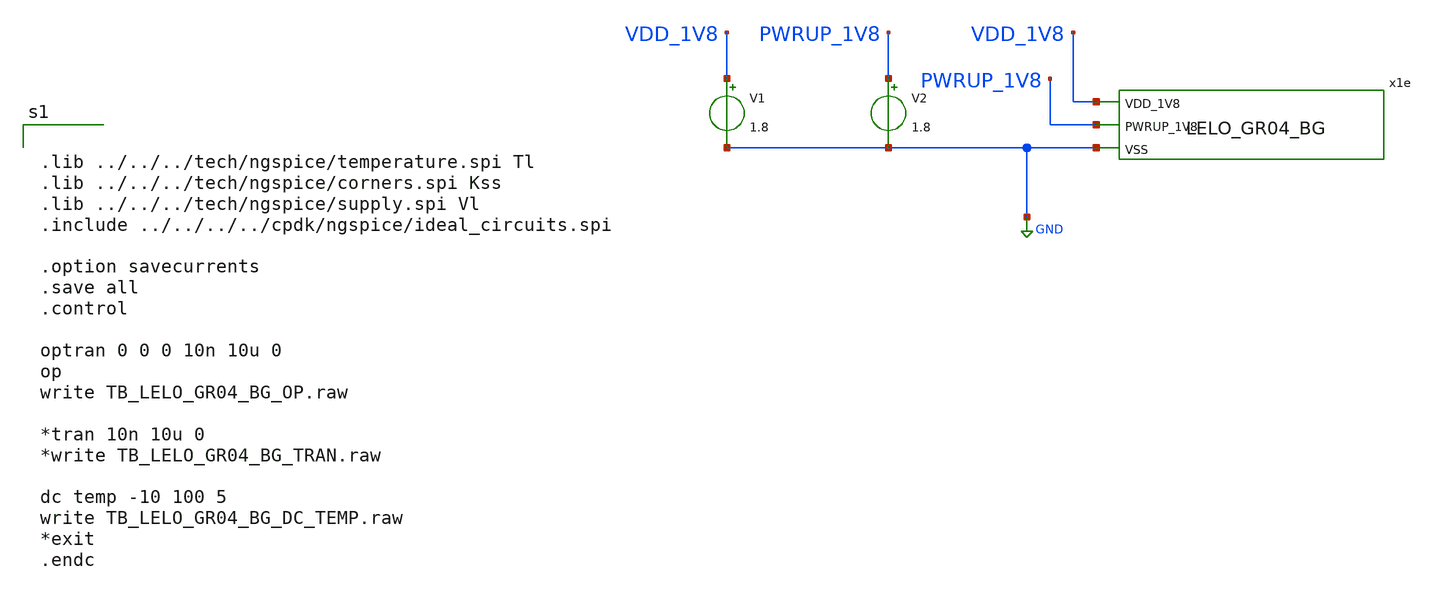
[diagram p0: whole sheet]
** sch_path: design/LELO_GR04_SKY130A/TB_LELO_GR04_BG.sch
**.subckt TB_LELO_GR04_BG
x1e VDD_1V8 PWRUP_1V8 GND LELO_GR04_BG
V1 VDD_1V8 GND 1.8
V2 PWRUP_1V8 GND 1.8
**** begin user architecture code


.lib ../../../tech/ngspice/temperature.spi Tl
.lib ../../../tech/ngspice/corners.spi Kss
.lib ../../../tech/ngspice/supply.spi Vl
.include ../../../../cpdk/ngspice/ideal_circuits.spi

.option savecurrents
.save all
.control

optran 0 0 0 10n 10u 0
op
write TB_LELO_GR04_BG_OP.raw

*tran 10n 10u 0
*write TB_LELO_GR04_BG_TRAN.raw

dc temp -10 100 5
write TB_LELO_GR04_BG_DC_TEMP.raw
*exit
.endc


**** end user architecture code
**.ends
.GLOBAL GND
.end
